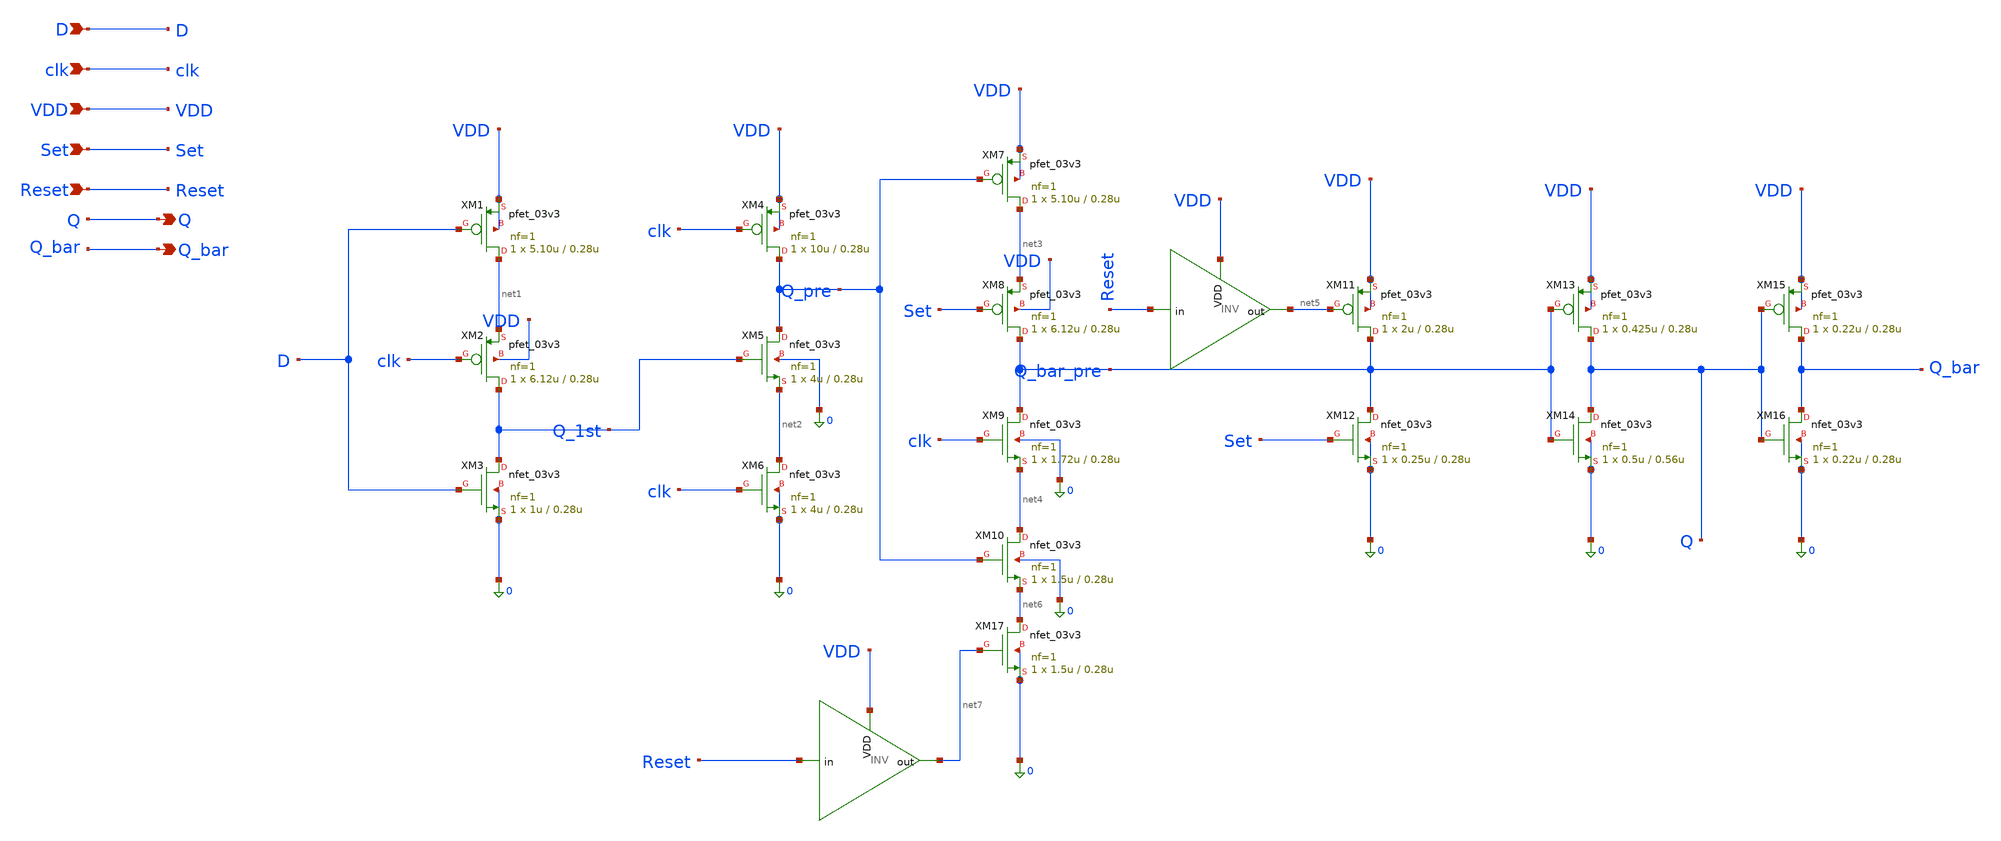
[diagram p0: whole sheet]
** sch_path: Design_Files/IC Design/Schematic/SAR_ADC_BLOCKS/TSPC_FF/TSPC_FF.sch
**.subckt TSPC_FF D clk VDD Set Reset Q Q_bar
*.ipin D
*.ipin clk
*.ipin VDD
*.ipin Set
*.ipin Reset
*.opin Q
*.opin Q_bar
XM1 net1 D VDD VDD pfet_03v3 L=0.28u W=5.10u nf=1 ad='int((nf+1)/2) * W/nf * 0.18u' as='int((nf+2)/2) * W/nf * 0.18u'
+ pd='2*int((nf+1)/2) * (W/nf + 0.18u)' ps='2*int((nf+2)/2) * (W/nf + 0.18u)' nrd='0.18u / W' nrs='0.18u / W'
+ sa=0 sb=0 sd=0 m=1
XM2 Q_1st clk net1 VDD pfet_03v3 L=0.28u W=6.12u nf=1 ad='int((nf+1)/2) * W/nf * 0.18u' as='int((nf+2)/2) * W/nf * 0.18u'
+ pd='2*int((nf+1)/2) * (W/nf + 0.18u)' ps='2*int((nf+2)/2) * (W/nf + 0.18u)' nrd='0.18u / W' nrs='0.18u / W'
+ sa=0 sb=0 sd=0 m=1
XM3 Q_1st D 0 0 nfet_03v3 L=0.28u W=1u nf=1 ad='int((nf+1)/2) * W/nf * 0.18u' as='int((nf+2)/2) * W/nf * 0.18u'
+ pd='2*int((nf+1)/2) * (W/nf + 0.18u)' ps='2*int((nf+2)/2) * (W/nf + 0.18u)' nrd='0.18u / W' nrs='0.18u / W'
+ sa=0 sb=0 sd=0 m=1
XM4 Q_pre clk VDD VDD pfet_03v3 L=0.28u W=10u nf=1 ad='int((nf+1)/2) * W/nf * 0.18u' as='int((nf+2)/2) * W/nf * 0.18u'
+ pd='2*int((nf+1)/2) * (W/nf + 0.18u)' ps='2*int((nf+2)/2) * (W/nf + 0.18u)' nrd='0.18u / W' nrs='0.18u / W'
+ sa=0 sb=0 sd=0 m=1
XM6 net2 clk 0 0 nfet_03v3 L=0.28u W=4u nf=1 ad='int((nf+1)/2) * W/nf * 0.18u' as='int((nf+2)/2) * W/nf * 0.18u'
+ pd='2*int((nf+1)/2) * (W/nf + 0.18u)' ps='2*int((nf+2)/2) * (W/nf + 0.18u)' nrd='0.18u / W' nrs='0.18u / W'
+ sa=0 sb=0 sd=0 m=1
XM7 net3 Q_pre VDD VDD pfet_03v3 L=0.28u W=5.10u nf=1 ad='int((nf+1)/2) * W/nf * 0.18u' as='int((nf+2)/2) * W/nf * 0.18u'
+ pd='2*int((nf+1)/2) * (W/nf + 0.18u)' ps='2*int((nf+2)/2) * (W/nf + 0.18u)' nrd='0.18u / W' nrs='0.18u / W'
+ sa=0 sb=0 sd=0 m=1
XM8 Q_bar_pre Set net3 VDD pfet_03v3 L=0.28u W=6.12u nf=1 ad='int((nf+1)/2) * W/nf * 0.18u' as='int((nf+2)/2) * W/nf * 0.18u'
+ pd='2*int((nf+1)/2) * (W/nf + 0.18u)' ps='2*int((nf+2)/2) * (W/nf + 0.18u)' nrd='0.18u / W' nrs='0.18u / W'
+ sa=0 sb=0 sd=0 m=1
XM9 Q_bar_pre clk net4 0 nfet_03v3 L=0.28u W=1.72u nf=1 ad='int((nf+1)/2) * W/nf * 0.18u' as='int((nf+2)/2) * W/nf * 0.18u'
+ pd='2*int((nf+1)/2) * (W/nf + 0.18u)' ps='2*int((nf+2)/2) * (W/nf + 0.18u)' nrd='0.18u / W' nrs='0.18u / W'
+ sa=0 sb=0 sd=0 m=1
XM10 net4 Q_pre net6 0 nfet_03v3 L=0.28u W=1.5u nf=1 ad='int((nf+1)/2) * W/nf * 0.18u' as='int((nf+2)/2) * W/nf * 0.18u'
+ pd='2*int((nf+1)/2) * (W/nf + 0.18u)' ps='2*int((nf+2)/2) * (W/nf + 0.18u)' nrd='0.18u / W' nrs='0.18u / W'
+ sa=0 sb=0 sd=0 m=1
XM11 Q_bar_pre net5 VDD VDD pfet_03v3 L=0.28u W=2u nf=1 ad='int((nf+1)/2) * W/nf * 0.18u' as='int((nf+2)/2) * W/nf * 0.18u'
+ pd='2*int((nf+1)/2) * (W/nf + 0.18u)' ps='2*int((nf+2)/2) * (W/nf + 0.18u)' nrd='0.18u / W' nrs='0.18u / W'
+ sa=0 sb=0 sd=0 m=1
XM12 Q_bar_pre Set 0 0 nfet_03v3 L=0.28u W=0.25u nf=1 ad='int((nf+1)/2) * W/nf * 0.18u' as='int((nf+2)/2) * W/nf * 0.18u'
+ pd='2*int((nf+1)/2) * (W/nf + 0.18u)' ps='2*int((nf+2)/2) * (W/nf + 0.18u)' nrd='0.18u / W' nrs='0.18u / W'
+ sa=0 sb=0 sd=0 m=1
XM13 Q Q_bar_pre VDD VDD pfet_03v3 L=0.28u W=0.425u nf=1 ad='int((nf+1)/2) * W/nf * 0.18u' as='int((nf+2)/2) * W/nf * 0.18u'
+ pd='2*int((nf+1)/2) * (W/nf + 0.18u)' ps='2*int((nf+2)/2) * (W/nf + 0.18u)' nrd='0.18u / W' nrs='0.18u / W'
+ sa=0 sb=0 sd=0 m=1
XM14 Q Q_bar_pre 0 0 nfet_03v3 L=0.56u W=0.5u nf=1 ad='int((nf+1)/2) * W/nf * 0.18u' as='int((nf+2)/2) * W/nf * 0.18u'
+ pd='2*int((nf+1)/2) * (W/nf + 0.18u)' ps='2*int((nf+2)/2) * (W/nf + 0.18u)' nrd='0.18u / W' nrs='0.18u / W'
+ sa=0 sb=0 sd=0 m=1
XM15 Q_bar Q VDD VDD pfet_03v3 L=0.28u W=0.22u nf=1 ad='int((nf+1)/2) * W/nf * 0.18u' as='int((nf+2)/2) * W/nf * 0.18u'
+ pd='2*int((nf+1)/2) * (W/nf + 0.18u)' ps='2*int((nf+2)/2) * (W/nf + 0.18u)' nrd='0.18u / W' nrs='0.18u / W'
+ sa=0 sb=0 sd=0 m=1
XM16 Q_bar Q 0 0 nfet_03v3 L=0.28u W=0.22u nf=1 ad='int((nf+1)/2) * W/nf * 0.18u' as='int((nf+2)/2) * W/nf * 0.18u'
+ pd='2*int((nf+1)/2) * (W/nf + 0.18u)' ps='2*int((nf+2)/2) * (W/nf + 0.18u)' nrd='0.18u / W' nrs='0.18u / W'
+ sa=0 sb=0 sd=0 m=1
XM17 net6 net7 0 0 nfet_03v3 L=0.28u W=1.5u nf=1 ad='int((nf+1)/2) * W/nf * 0.18u' as='int((nf+2)/2) * W/nf * 0.18u'
+ pd='2*int((nf+1)/2) * (W/nf + 0.18u)' ps='2*int((nf+2)/2) * (W/nf + 0.18u)' nrd='0.18u / W' nrs='0.18u / W'
+ sa=0 sb=0 sd=0 m=1
xINV1_1 Reset VDD net7 INV
xINV1_2 Reset VDD net5 INV
XM5 Q_pre Q_1st net2 0 nfet_03v3 L=0.28u W=4u nf=1 ad='int((nf+1)/2) * W/nf * 0.18u' as='int((nf+2)/2) * W/nf * 0.18u'
+ pd='2*int((nf+1)/2) * (W/nf + 0.18u)' ps='2*int((nf+2)/2) * (W/nf + 0.18u)' nrd='0.18u / W' nrs='0.18u / W'
+ sa=0 sb=0 sd=0 m=1
**.ends

* expanding   symbol:  ECG_Acquisition_IC/Design_Files/IC
*+ Design/Schematic/SAR_ADC_BLOCKS/INV/INV.sym # of pins=3
** sym_path: Design_Files/IC Design/Schematic/SAR_ADC_BLOCKS/INV/INV.sym
** sch_path: Design_Files/IC Design/Schematic/SAR_ADC_BLOCKS/INV/INV.sch
.subckt INV in VDD out
*.ipin in
*.ipin VDD
*.opin out
XM1 out in 0 0 nfet_03v3 L=0.28u W=0.22u nf=1 ad='int((nf+1)/2) * W/nf * 0.18u' as='int((nf+2)/2) * W/nf * 0.18u'
+ pd='2*int((nf+1)/2) * (W/nf + 0.18u)' ps='2*int((nf+2)/2) * (W/nf + 0.18u)' nrd='0.18u / W' nrs='0.18u / W'
+ sa=0 sb=0 sd=0 m=wn_inv
XM2 out in vdd vdd pfet_03v3 L=0.28u W=0.22u nf=1 ad='int((nf+1)/2) * W/nf * 0.18u' as='int((nf+2)/2) * W/nf * 0.18u'
+ pd='2*int((nf+1)/2) * (W/nf + 0.18u)' ps='2*int((nf+2)/2) * (W/nf + 0.18u)' nrd='0.18u / W' nrs='0.18u / W'
+ sa=0 sb=0 sd=0 m=wp_inv
.ends

.end
